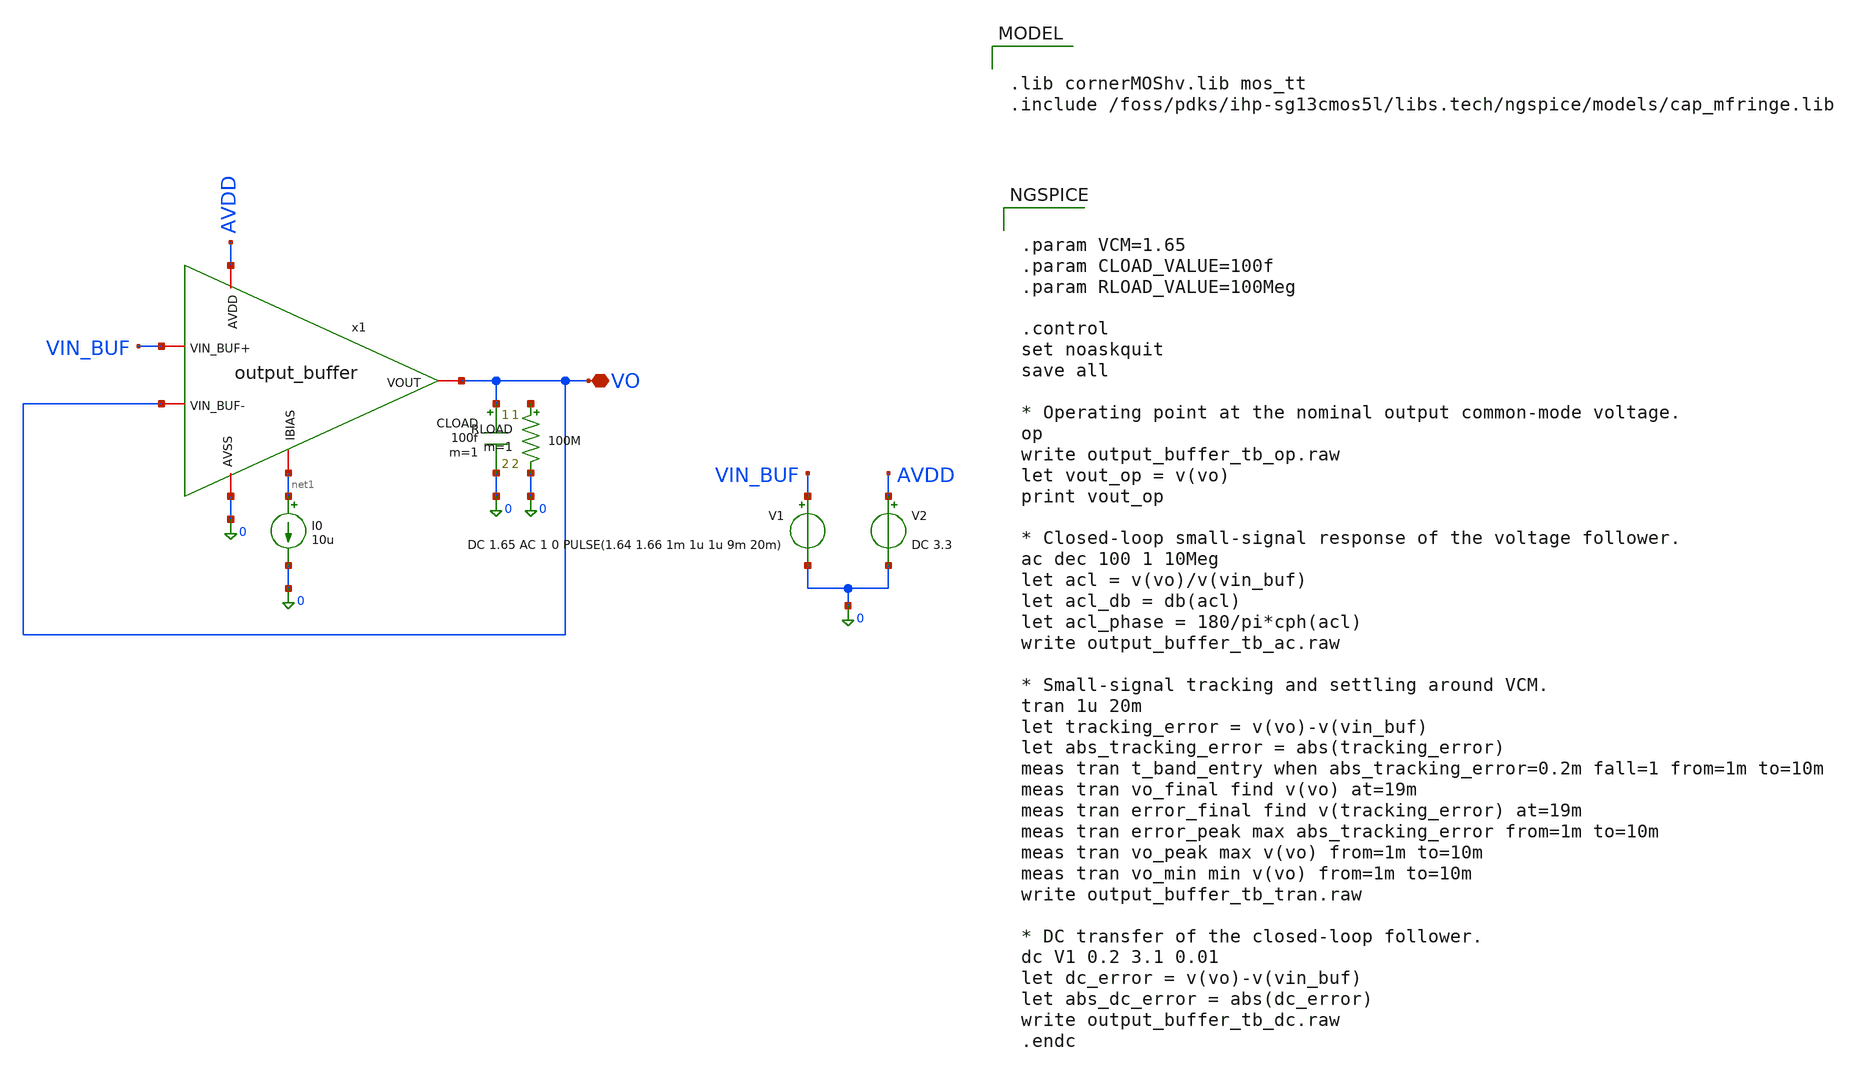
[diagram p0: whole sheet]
** sch_path: designs/libs/core_analog/output_buffer/output_buffer_tb.sch
**.subckt output_buffer_tb VO
*.iopin VO
V1 VIN_BUF 0 DC 1.65 AC 1 0 PULSE(1.64 1.66 1m 1u 1u 9m 20m)
V2 AVDD 0 DC 3.3
CLOAD VO 0 100f m=1
I0 net1 0 10u
x1 AVDD net1 VO VIN_BUF VO 0 output_buffer
RLOAD net2 0 100M m=1
**** begin user architecture code

.lib cornerMOShv.lib mos_tt
.include /foss/pdks/ihp-sg13cmos5l/libs.tech/ngspice/models/cap_mfringe.lib



.param VCM=1.65
.param CLOAD_VALUE=100f
.param RLOAD_VALUE=100Meg

.control
set noaskquit
save all

* Operating point at the nominal output common-mode voltage.
op
write output_buffer_tb_op.raw
let vout_op = v(vo)
print vout_op

* Closed-loop small-signal response of the voltage follower.
ac dec 100 1 10Meg
let acl = v(vo)/v(vin_buf)
let acl_db = db(acl)
let acl_phase = 180/pi*cph(acl)
write output_buffer_tb_ac.raw

* Small-signal tracking and settling around VCM.
tran 1u 20m
let tracking_error = v(vo)-v(vin_buf)
let abs_tracking_error = abs(tracking_error)
meas tran t_band_entry when abs_tracking_error=0.2m fall=1 from=1m to=10m
meas tran vo_final find v(vo) at=19m
meas tran error_final find v(tracking_error) at=19m
meas tran error_peak max abs_tracking_error from=1m to=10m
meas tran vo_peak max v(vo) from=1m to=10m
meas tran vo_min min v(vo) from=1m to=10m
write output_buffer_tb_tran.raw

* DC transfer of the closed-loop follower.
dc V1 0.2 3.1 0.01
let dc_error = v(vo)-v(vin_buf)
let abs_dc_error = abs(dc_error)
write output_buffer_tb_dc.raw
.endc


**** end user architecture code
**.ends
.end
